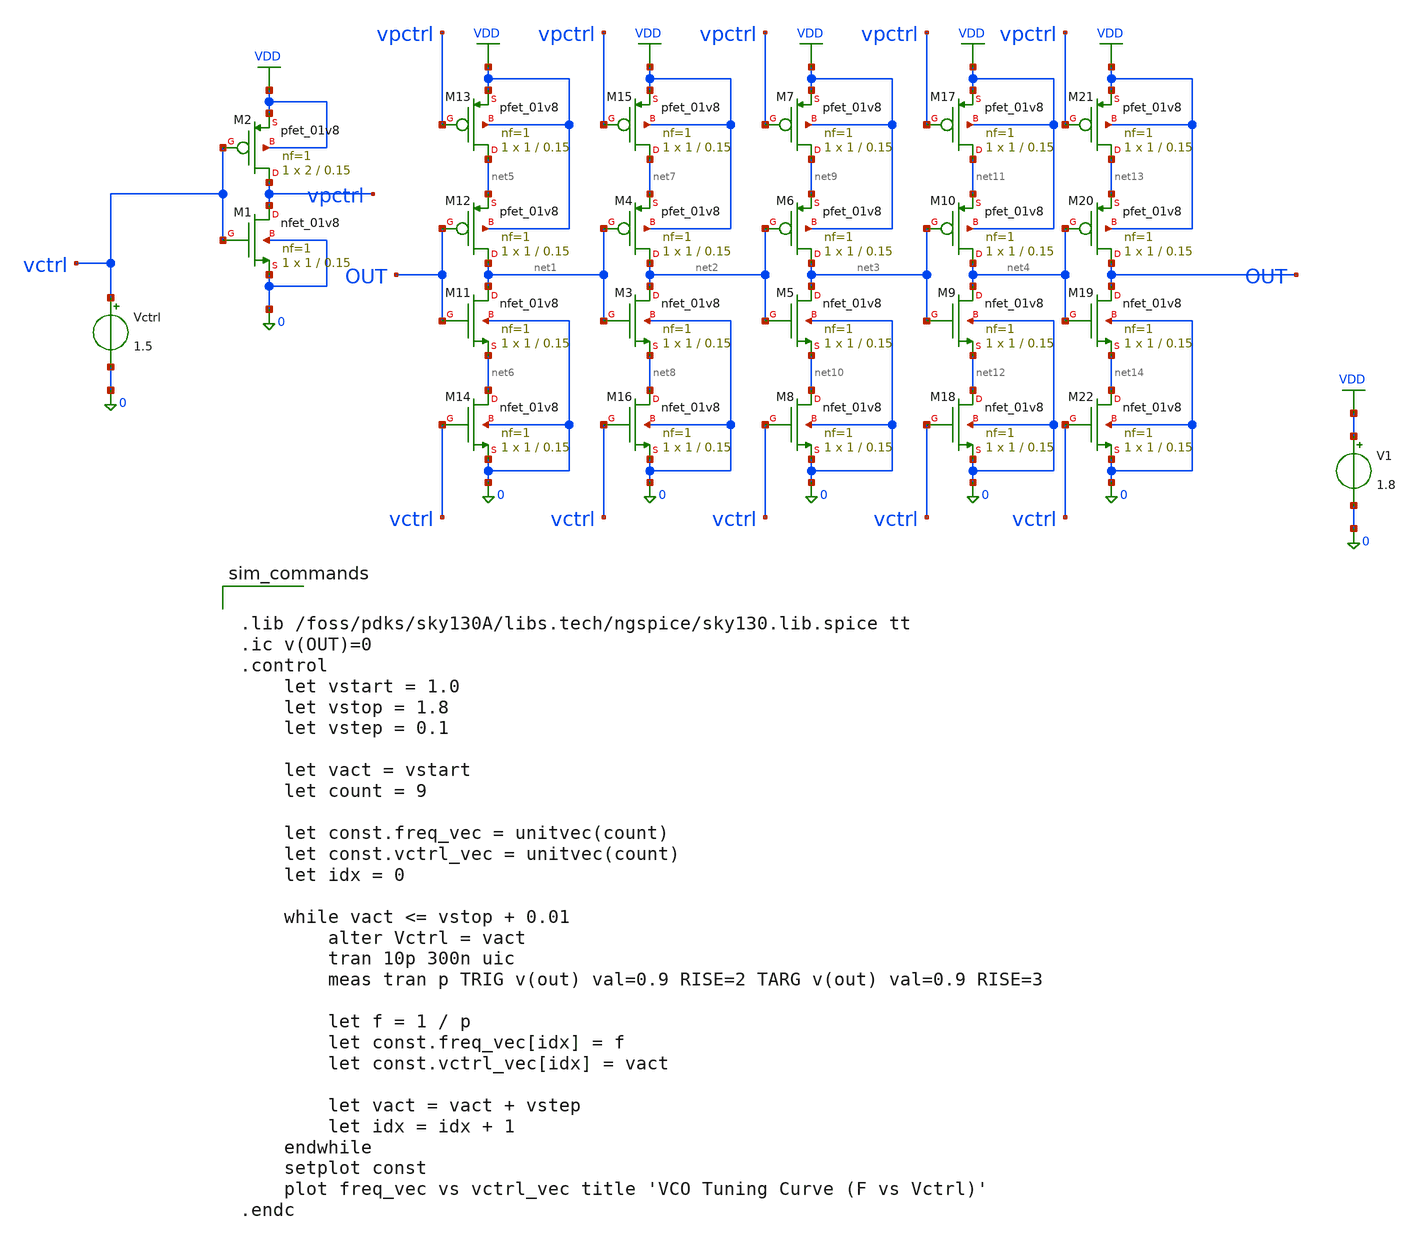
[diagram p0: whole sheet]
** sch_path: vco_tb.sch
**.subckt vco_tb
XM1 vpctrl vctrl 0 0 sky130_fd_pr__nfet_01v8 L=0.15 W=1 nf=1 ad='int((1 + 1)/2) * 1 / 1 * 0.29' as='int((1 + 2)/2) * 1 / 1 * 0.29'
+ pd='2*int((1 + 1)/2) * (1 / 1 + 0.29)' ps='2*int((1 + 2)/2) * (1 / 1 + 0.29)' nrd='0.29 / 1 ' nrs='0.29 / 1 '
+ sa=0 sb=0 sd=0 mult=1 m=1
XM2 vpctrl vctrl VDD VDD sky130_fd_pr__pfet_01v8 L=0.15 W=2 nf=1 ad='int((1 + 1)/2) * 2 / 1 * 0.29' as='int((1 + 2)/2) * 2 / 1 * 0.29'
+ pd='2*int((1 + 1)/2) * (2 / 1 + 0.29)' ps='2*int((1 + 2)/2) * (2 / 1 + 0.29)' nrd='0.29 / 2 ' nrs='0.29 / 2 '
+ sa=0 sb=0 sd=0 mult=1 m=1
V1 VDD 0 1.8
XM11 net1 OUT net6 0 sky130_fd_pr__nfet_01v8 L=0.15 W=1 nf=1 ad='int((1 + 1)/2) * 1 / 1 * 0.29' as='int((1 + 2)/2) * 1 / 1 * 0.29'
+ pd='2*int((1 + 1)/2) * (1 / 1 + 0.29)' ps='2*int((1 + 2)/2) * (1 / 1 + 0.29)' nrd='0.29 / 1 ' nrs='0.29 / 1 '
+ sa=0 sb=0 sd=0 mult=1 m=1
XM12 net1 OUT net5 VDD sky130_fd_pr__pfet_01v8 L=0.15 W=1 nf=1 ad='int((1 + 1)/2) * 1 / 1 * 0.29' as='int((1 + 2)/2) * 1 / 1 * 0.29'
+ pd='2*int((1 + 1)/2) * (1 / 1 + 0.29)' ps='2*int((1 + 2)/2) * (1 / 1 + 0.29)' nrd='0.29 / 1 ' nrs='0.29 / 1 '
+ sa=0 sb=0 sd=0 mult=1 m=1
XM13 net5 vpctrl VDD VDD sky130_fd_pr__pfet_01v8 L=0.15 W=1 nf=1 ad='int((1 + 1)/2) * 1 / 1 * 0.29' as='int((1 + 2)/2) * 1 / 1 * 0.29'
+ pd='2*int((1 + 1)/2) * (1 / 1 + 0.29)' ps='2*int((1 + 2)/2) * (1 / 1 + 0.29)' nrd='0.29 / 1 ' nrs='0.29 / 1 '
+ sa=0 sb=0 sd=0 mult=1 m=1
XM14 net6 vctrl 0 0 sky130_fd_pr__nfet_01v8 L=0.15 W=1 nf=1 ad='int((1 + 1)/2) * 1 / 1 * 0.29' as='int((1 + 2)/2) * 1 / 1 * 0.29'
+ pd='2*int((1 + 1)/2) * (1 / 1 + 0.29)' ps='2*int((1 + 2)/2) * (1 / 1 + 0.29)' nrd='0.29 / 1 ' nrs='0.29 / 1 '
+ sa=0 sb=0 sd=0 mult=1 m=1
XM3 net2 net1 net8 0 sky130_fd_pr__nfet_01v8 L=0.15 W=1 nf=1 ad='int((1 + 1)/2) * 1 / 1 * 0.29' as='int((1 + 2)/2) * 1 / 1 * 0.29'
+ pd='2*int((1 + 1)/2) * (1 / 1 + 0.29)' ps='2*int((1 + 2)/2) * (1 / 1 + 0.29)' nrd='0.29 / 1 ' nrs='0.29 / 1 '
+ sa=0 sb=0 sd=0 mult=1 m=1
XM4 net2 net1 net7 VDD sky130_fd_pr__pfet_01v8 L=0.15 W=1 nf=1 ad='int((1 + 1)/2) * 1 / 1 * 0.29' as='int((1 + 2)/2) * 1 / 1 * 0.29'
+ pd='2*int((1 + 1)/2) * (1 / 1 + 0.29)' ps='2*int((1 + 2)/2) * (1 / 1 + 0.29)' nrd='0.29 / 1 ' nrs='0.29 / 1 '
+ sa=0 sb=0 sd=0 mult=1 m=1
XM15 net7 vpctrl VDD VDD sky130_fd_pr__pfet_01v8 L=0.15 W=1 nf=1 ad='int((1 + 1)/2) * 1 / 1 * 0.29' as='int((1 + 2)/2) * 1 / 1 * 0.29'
+ pd='2*int((1 + 1)/2) * (1 / 1 + 0.29)' ps='2*int((1 + 2)/2) * (1 / 1 + 0.29)' nrd='0.29 / 1 ' nrs='0.29 / 1 '
+ sa=0 sb=0 sd=0 mult=1 m=1
XM16 net8 vctrl 0 0 sky130_fd_pr__nfet_01v8 L=0.15 W=1 nf=1 ad='int((1 + 1)/2) * 1 / 1 * 0.29' as='int((1 + 2)/2) * 1 / 1 * 0.29'
+ pd='2*int((1 + 1)/2) * (1 / 1 + 0.29)' ps='2*int((1 + 2)/2) * (1 / 1 + 0.29)' nrd='0.29 / 1 ' nrs='0.29 / 1 '
+ sa=0 sb=0 sd=0 mult=1 m=1
XM5 net3 net2 net10 0 sky130_fd_pr__nfet_01v8 L=0.15 W=1 nf=1 ad='int((1 + 1)/2) * 1 / 1 * 0.29' as='int((1 + 2)/2) * 1 / 1 * 0.29'
+ pd='2*int((1 + 1)/2) * (1 / 1 + 0.29)' ps='2*int((1 + 2)/2) * (1 / 1 + 0.29)' nrd='0.29 / 1 ' nrs='0.29 / 1 '
+ sa=0 sb=0 sd=0 mult=1 m=1
XM6 net3 net2 net9 VDD sky130_fd_pr__pfet_01v8 L=0.15 W=1 nf=1 ad='int((1 + 1)/2) * 1 / 1 * 0.29' as='int((1 + 2)/2) * 1 / 1 * 0.29'
+ pd='2*int((1 + 1)/2) * (1 / 1 + 0.29)' ps='2*int((1 + 2)/2) * (1 / 1 + 0.29)' nrd='0.29 / 1 ' nrs='0.29 / 1 '
+ sa=0 sb=0 sd=0 mult=1 m=1
XM7 net9 vpctrl VDD VDD sky130_fd_pr__pfet_01v8 L=0.15 W=1 nf=1 ad='int((1 + 1)/2) * 1 / 1 * 0.29' as='int((1 + 2)/2) * 1 / 1 * 0.29'
+ pd='2*int((1 + 1)/2) * (1 / 1 + 0.29)' ps='2*int((1 + 2)/2) * (1 / 1 + 0.29)' nrd='0.29 / 1 ' nrs='0.29 / 1 '
+ sa=0 sb=0 sd=0 mult=1 m=1
XM8 net10 vctrl 0 0 sky130_fd_pr__nfet_01v8 L=0.15 W=1 nf=1 ad='int((1 + 1)/2) * 1 / 1 * 0.29' as='int((1 + 2)/2) * 1 / 1 * 0.29'
+ pd='2*int((1 + 1)/2) * (1 / 1 + 0.29)' ps='2*int((1 + 2)/2) * (1 / 1 + 0.29)' nrd='0.29 / 1 ' nrs='0.29 / 1 '
+ sa=0 sb=0 sd=0 mult=1 m=1
XM9 net4 net3 net12 0 sky130_fd_pr__nfet_01v8 L=0.15 W=1 nf=1 ad='int((1 + 1)/2) * 1 / 1 * 0.29' as='int((1 + 2)/2) * 1 / 1 * 0.29'
+ pd='2*int((1 + 1)/2) * (1 / 1 + 0.29)' ps='2*int((1 + 2)/2) * (1 / 1 + 0.29)' nrd='0.29 / 1 ' nrs='0.29 / 1 '
+ sa=0 sb=0 sd=0 mult=1 m=1
XM10 net4 net3 net11 VDD sky130_fd_pr__pfet_01v8 L=0.15 W=1 nf=1 ad='int((1 + 1)/2) * 1 / 1 * 0.29' as='int((1 + 2)/2) * 1 / 1 * 0.29'
+ pd='2*int((1 + 1)/2) * (1 / 1 + 0.29)' ps='2*int((1 + 2)/2) * (1 / 1 + 0.29)' nrd='0.29 / 1 ' nrs='0.29 / 1 '
+ sa=0 sb=0 sd=0 mult=1 m=1
XM17 net11 vpctrl VDD VDD sky130_fd_pr__pfet_01v8 L=0.15 W=1 nf=1 ad='int((1 + 1)/2) * 1 / 1 * 0.29'
+ as='int((1 + 2)/2) * 1 / 1 * 0.29' pd='2*int((1 + 1)/2) * (1 / 1 + 0.29)' ps='2*int((1 + 2)/2) * (1 / 1 + 0.29)'
+ nrd='0.29 / 1 ' nrs='0.29 / 1 ' sa=0 sb=0 sd=0 mult=1 m=1
XM18 net12 vctrl 0 0 sky130_fd_pr__nfet_01v8 L=0.15 W=1 nf=1 ad='int((1 + 1)/2) * 1 / 1 * 0.29' as='int((1 + 2)/2) * 1 / 1 * 0.29'
+ pd='2*int((1 + 1)/2) * (1 / 1 + 0.29)' ps='2*int((1 + 2)/2) * (1 / 1 + 0.29)' nrd='0.29 / 1 ' nrs='0.29 / 1 '
+ sa=0 sb=0 sd=0 mult=1 m=1
XM19 OUT net4 net14 0 sky130_fd_pr__nfet_01v8 L=0.15 W=1 nf=1 ad='int((1 + 1)/2) * 1 / 1 * 0.29' as='int((1 + 2)/2) * 1 / 1 * 0.29'
+ pd='2*int((1 + 1)/2) * (1 / 1 + 0.29)' ps='2*int((1 + 2)/2) * (1 / 1 + 0.29)' nrd='0.29 / 1 ' nrs='0.29 / 1 '
+ sa=0 sb=0 sd=0 mult=1 m=1
XM20 OUT net4 net13 VDD sky130_fd_pr__pfet_01v8 L=0.15 W=1 nf=1 ad='int((1 + 1)/2) * 1 / 1 * 0.29' as='int((1 + 2)/2) * 1 / 1 * 0.29'
+ pd='2*int((1 + 1)/2) * (1 / 1 + 0.29)' ps='2*int((1 + 2)/2) * (1 / 1 + 0.29)' nrd='0.29 / 1 ' nrs='0.29 / 1 '
+ sa=0 sb=0 sd=0 mult=1 m=1
XM21 net13 vpctrl VDD VDD sky130_fd_pr__pfet_01v8 L=0.15 W=1 nf=1 ad='int((1 + 1)/2) * 1 / 1 * 0.29'
+ as='int((1 + 2)/2) * 1 / 1 * 0.29' pd='2*int((1 + 1)/2) * (1 / 1 + 0.29)' ps='2*int((1 + 2)/2) * (1 / 1 + 0.29)'
+ nrd='0.29 / 1 ' nrs='0.29 / 1 ' sa=0 sb=0 sd=0 mult=1 m=1
XM22 net14 vctrl 0 0 sky130_fd_pr__nfet_01v8 L=0.15 W=1 nf=1 ad='int((1 + 1)/2) * 1 / 1 * 0.29' as='int((1 + 2)/2) * 1 / 1 * 0.29'
+ pd='2*int((1 + 1)/2) * (1 / 1 + 0.29)' ps='2*int((1 + 2)/2) * (1 / 1 + 0.29)' nrd='0.29 / 1 ' nrs='0.29 / 1 '
+ sa=0 sb=0 sd=0 mult=1 m=1
Vctrl vctrl 0 1.5
**** begin user architecture code


.lib /foss/pdks/sky130A/libs.tech/ngspice/sky130.lib.spice tt
.ic v(OUT)=0
.control
	let vstart = 1.0
	let vstop = 1.8
	let vstep = 0.1

	let vact = vstart
	let count = 9

	let const.freq_vec = unitvec(count)
	let const.vctrl_vec = unitvec(count)
	let idx = 0

	while vact <= vstop + 0.01
		alter Vctrl = vact
		tran 10p 300n uic
		meas tran p TRIG v(out) val=0.9 RISE=2 TARG v(out) val=0.9 RISE=3

		let f = 1 / p
		let const.freq_vec[idx] = f
		let const.vctrl_vec[idx] = vact

		let vact = vact + vstep
		let idx = idx + 1
	endwhile
	setplot const
	plot freq_vec vs vctrl_vec title 'VCO Tuning Curve (F vs Vctrl)'
.endc


OUT
**** end user architecture code
**.ends
.GLOBAL VDD
.end
